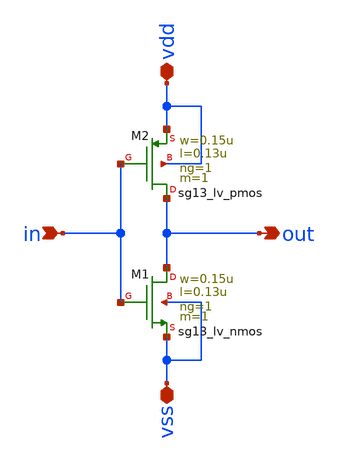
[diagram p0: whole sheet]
** sch_path: inverter/xschem/inverter.sch
**.subckt inverter vdd vss in out
*.iopin vdd
*.iopin vss
*.ipin in
*.opin out
XM1 out in vss vss sg13_lv_nmos w=0.15u l=0.13u ng=1 m=1 mm_ok=1
XM2 out in vdd vdd sg13_lv_pmos w=0.15u l=0.13u ng=1 m=1 mm_ok=1
**.ends
.end
